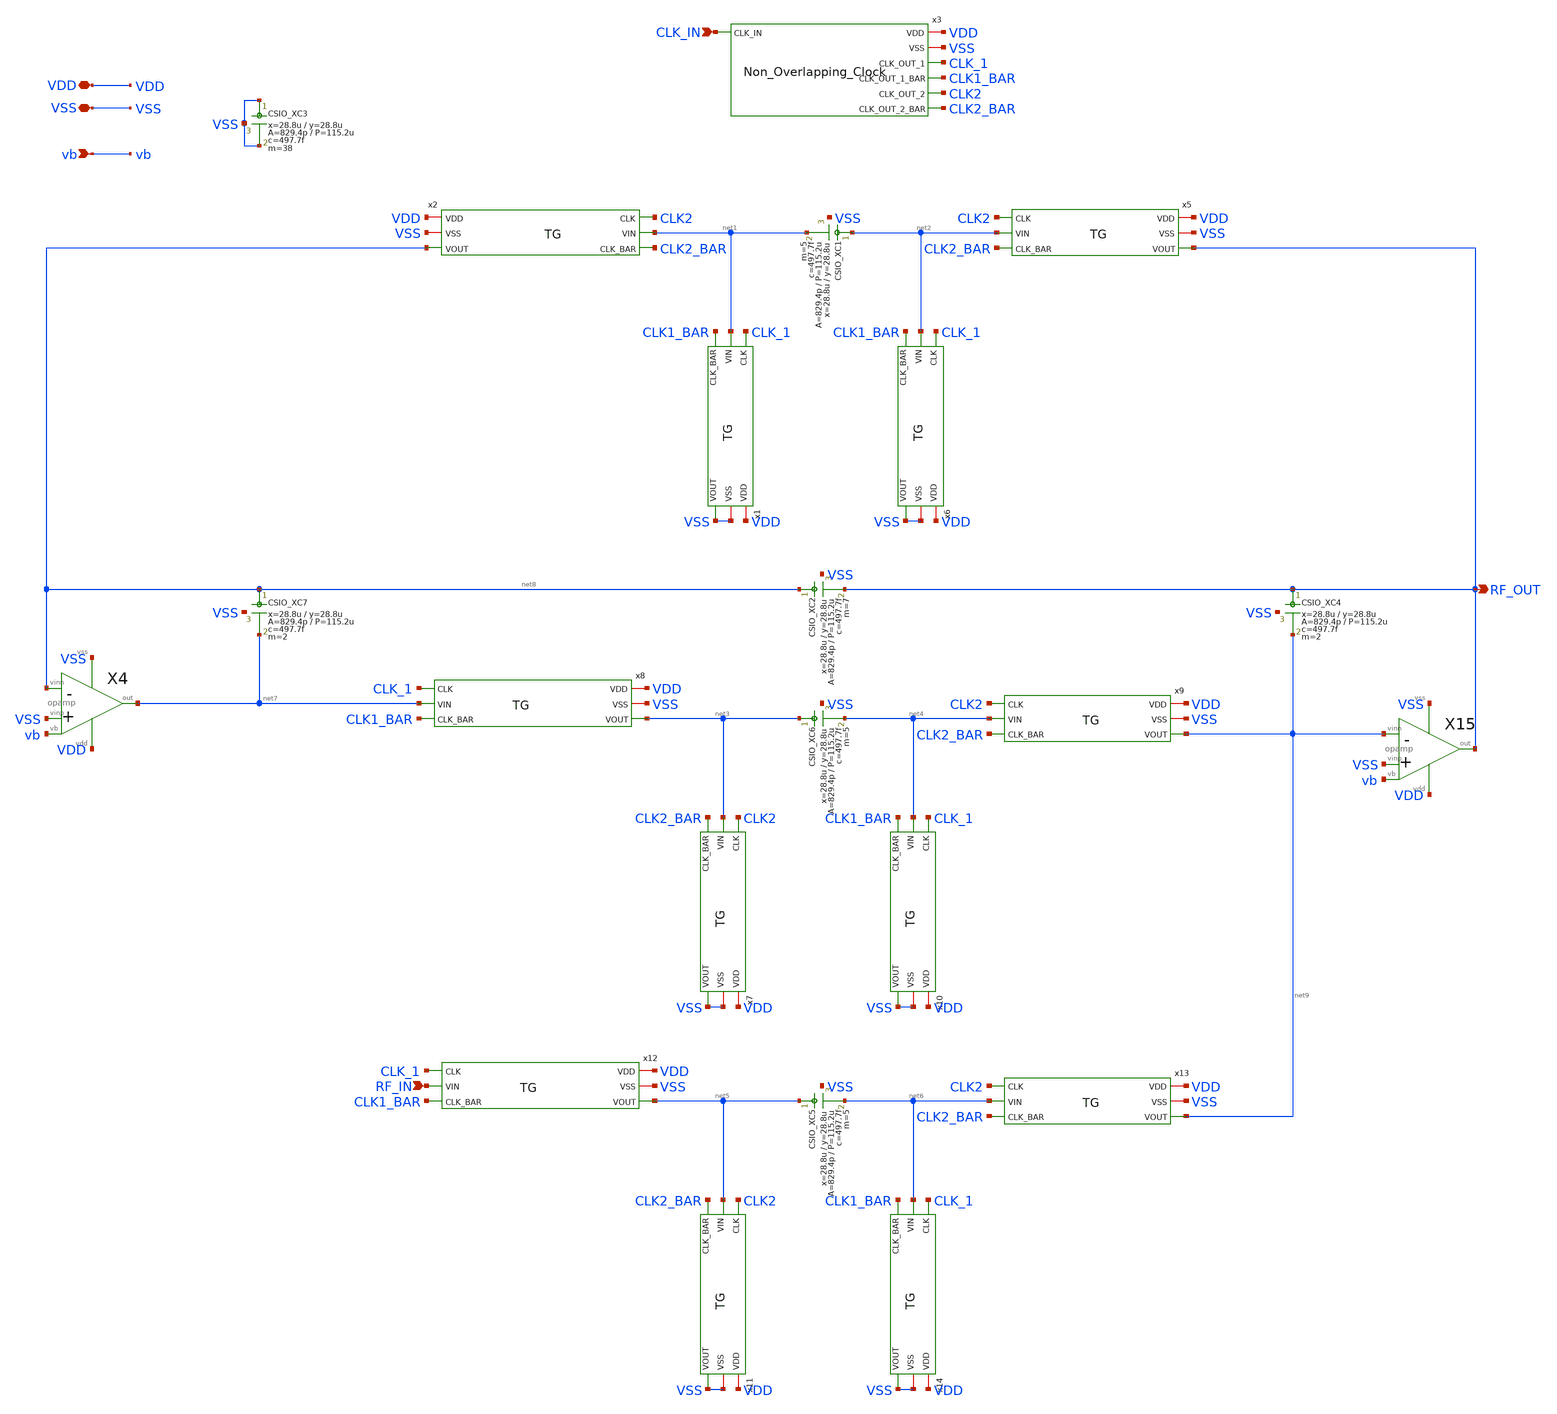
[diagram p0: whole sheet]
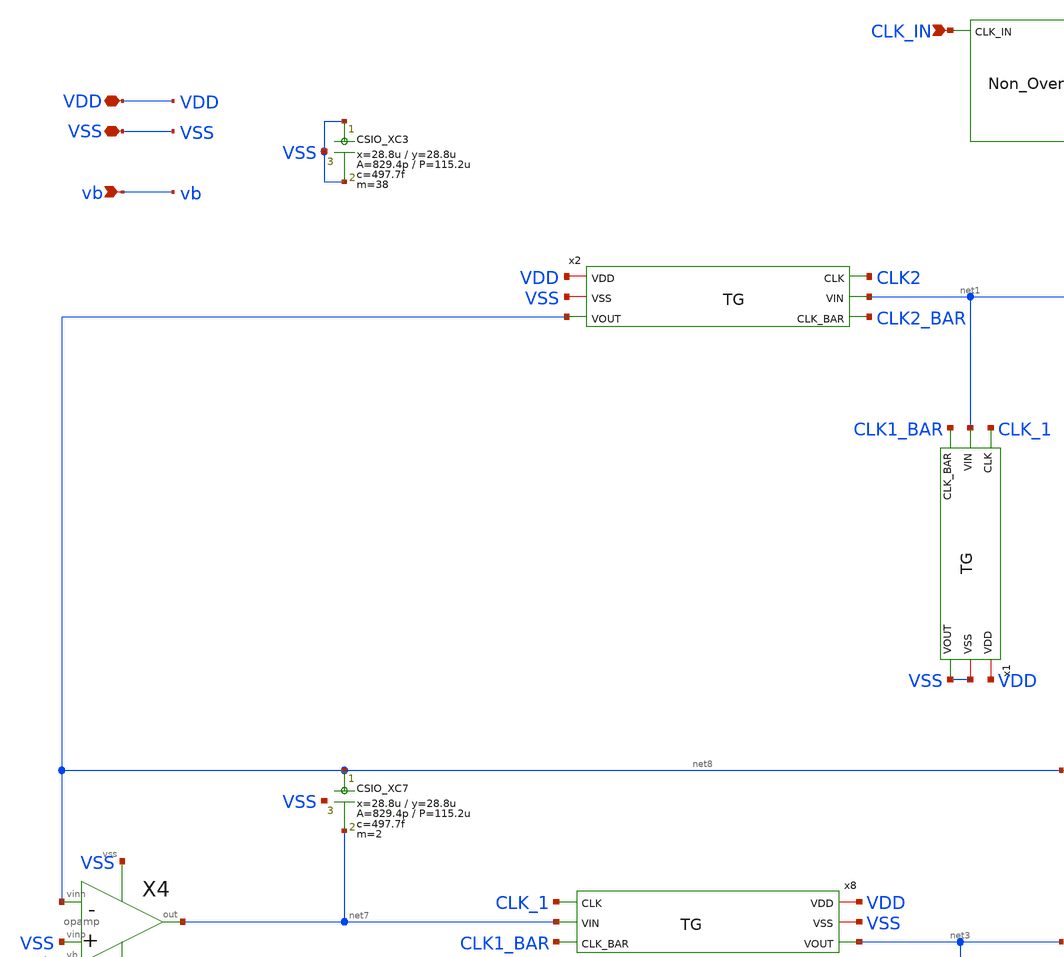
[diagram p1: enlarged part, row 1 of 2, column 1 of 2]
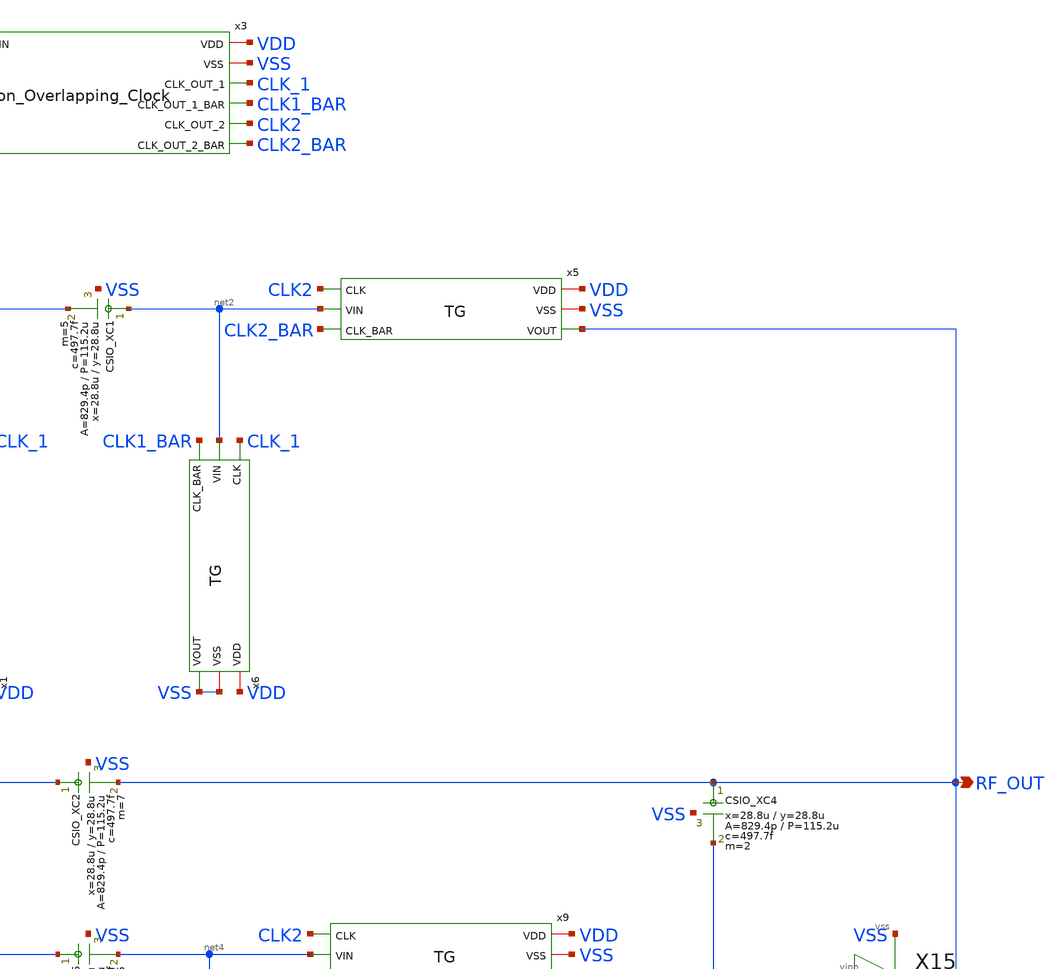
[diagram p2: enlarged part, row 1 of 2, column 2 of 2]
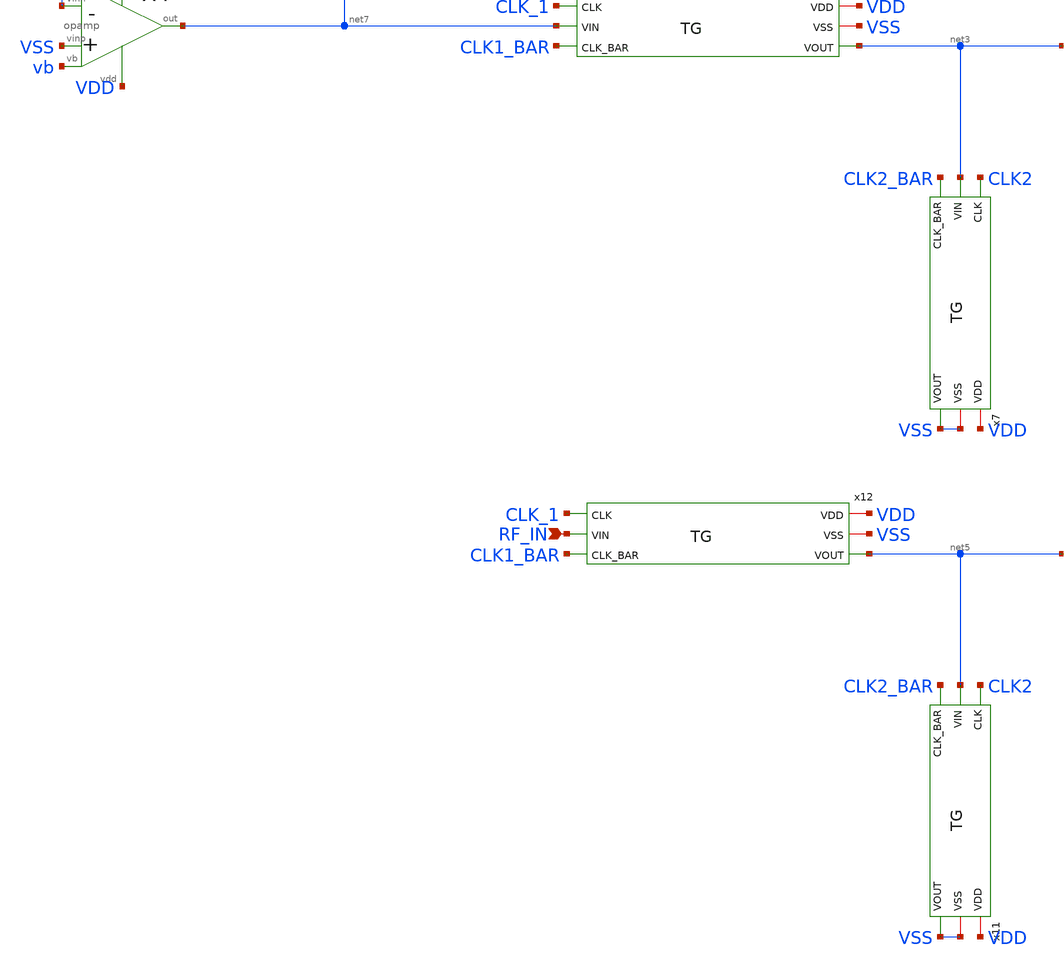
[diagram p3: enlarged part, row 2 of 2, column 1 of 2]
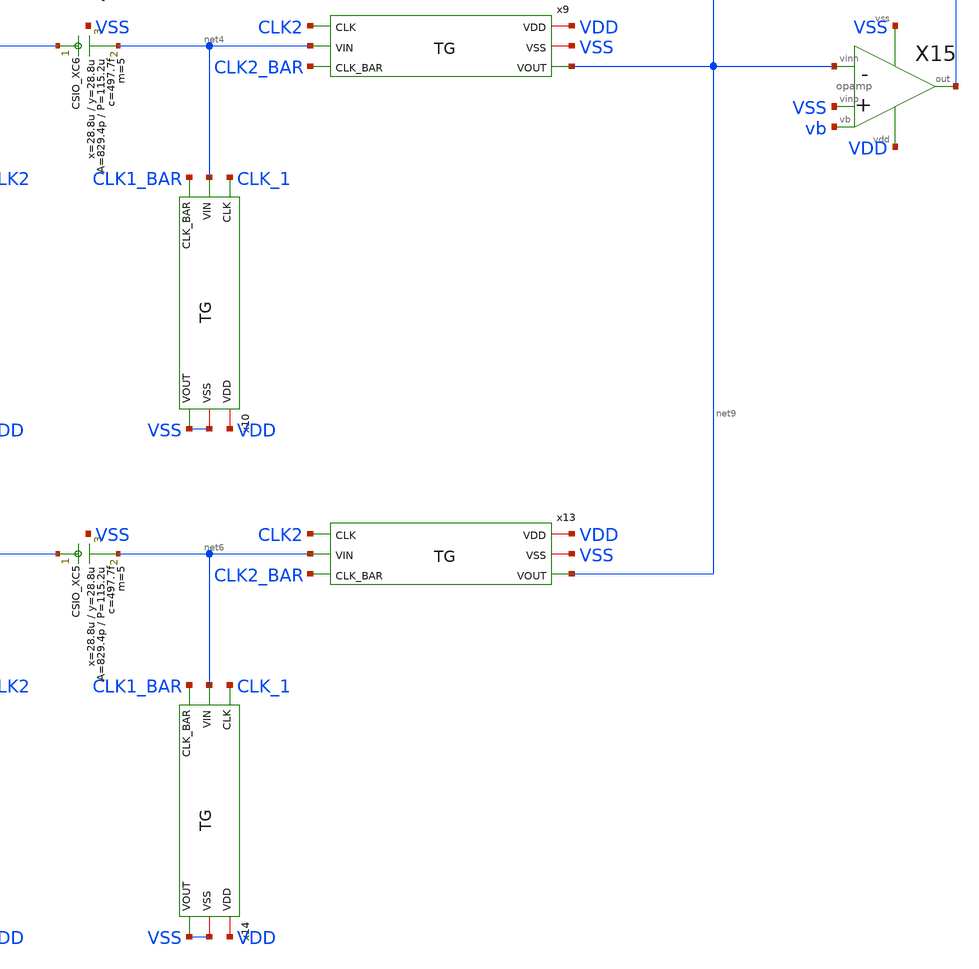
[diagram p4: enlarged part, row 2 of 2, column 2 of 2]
** sch_path: member_project/LPF/noritsuna/xschem/LPF.sch
**.subckt LPF VDD VSS vb CLK_IN RF_IN RF_OUT
*.iopin VDD
*.iopin VSS
*.ipin vb
*.ipin CLK_IN
*.ipin RF_IN
*.opin RF_OUT
x1 VDD VSS CLK_1 net1 VSS CLK1_BAR TG
x2 VDD VSS CLK2 net1 net8 CLK2_BAR TG
x3 VDD VSS CLK_IN CLK_1 CLK1_BAR CLK2 CLK2_BAR Non_Overlapping_Clock
X4 VSS net8 vb net7 VDD VSS opamp
x5 VDD VSS CLK2 net2 RF_OUT CLK2_BAR TG
x6 VDD VSS CLK_1 net2 VSS CLK1_BAR TG
x7 VDD VSS CLK2 net3 VSS CLK2_BAR TG
x8 VDD VSS CLK_1 net7 net3 CLK1_BAR TG
x9 VDD VSS CLK2 net4 net9 CLK2_BAR TG
x10 VDD VSS CLK_1 net4 VSS CLK1_BAR TG
x11 VDD VSS CLK2 net5 VSS CLK2_BAR TG
x13 VDD VSS CLK2 net6 net9 CLK2_BAR TG
x14 VDD VSS CLK_1 net6 VSS CLK1_BAR TG
x12 VDD VSS CLK_1 RF_IN net5 CLK1_BAR TG
XXC1 net2 net1 VSS F_CSIO c=497.7f x=28.8u y=28.8u m=5
XXC2 net8 RF_OUT VSS F_CSIO c=497.7f x=28.8u y=28.8u m=7
XXC3 VSS VSS VSS F_CSIO c=497.7f x=28.8u y=28.8u m=38
XXC4 RF_OUT net9 VSS F_CSIO c=497.7f x=28.8u y=28.8u m=2
XXC5 net5 net6 VSS F_CSIO c=497.7f x=28.8u y=28.8u m=5
XXC6 net3 net4 VSS F_CSIO c=497.7f x=28.8u y=28.8u m=5
X15 VSS net9 vb RF_OUT VDD VSS opamp
XXC7 net8 net7 VSS F_CSIO c=497.7f x=28.8u y=28.8u m=2
**.ends
.end
